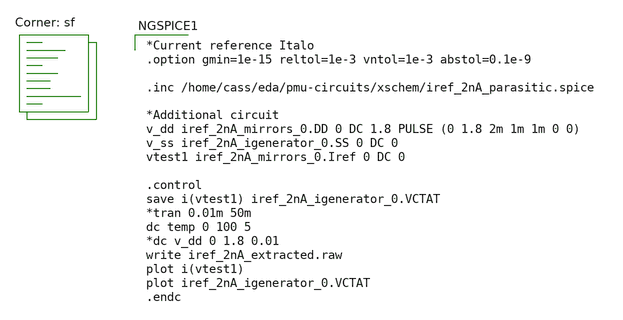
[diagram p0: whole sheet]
** sch_path: xschem/test_iref_2nA_extracted.sch
**.subckt test_iref_2nA_extracted
**** begin user architecture code
.lib $::SKYWATER_MODELS/sky130.lib.spice sf

*Current reference Italo
.option gmin=1e-15 reltol=1e-3 vntol=1e-3 abstol=0.1e-9

.inc /home/cass/eda/pmu-circuits/xschem/iref_2nA_parasitic.spice

*Additional circuit
v_dd iref_2nA_mirrors_0.DD 0 DC 1.8 PULSE (0 1.8 2m 1m 1m 0 0)
v_ss iref_2nA_igenerator_0.SS 0 DC 0
vtest1 iref_2nA_mirrors_0.Iref 0 DC 0

.control
save i(vtest1) iref_2nA_igenerator_0.VCTAT
*tran 0.01m 50m
dc temp 0 100 5
*dc v_dd 0 1.8 0.01
write iref_2nA_extracted.raw
plot i(vtest1)
plot iref_2nA_igenerator_0.VCTAT
.endc


**** end user architecture code
**.ends
.end
